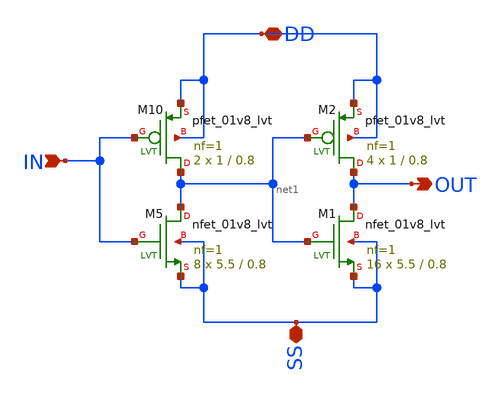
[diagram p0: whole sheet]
** sch_path: xschem/ring_100mV_buffer.sch
**.subckt ring_100mV_buffer OUT DD SS IN
*.opin OUT
*.iopin DD
*.iopin SS
*.ipin IN
XM5 net1 IN SS SS sky130_fd_pr__nfet_01v8_lvt L=0.8 W=5.5 nf=1 ad='int((nf+1)/2) * W/nf * 0.29' as='int((nf+2)/2) * W/nf * 0.29'
+ pd='2*int((nf+1)/2) * (W/nf + 0.29)' ps='2*int((nf+2)/2) * (W/nf + 0.29)' nrd='0.29 / W' nrs='0.29 / W'
+ sa=0 sb=0 sd=0 mult=8 m=8
XM10 net1 IN DD DD sky130_fd_pr__pfet_01v8_lvt L=0.8 W=1 nf=1 ad='int((nf+1)/2) * W/nf * 0.29' as='int((nf+2)/2) * W/nf * 0.29'
+ pd='2*int((nf+1)/2) * (W/nf + 0.29)' ps='2*int((nf+2)/2) * (W/nf + 0.29)' nrd='0.29 / W' nrs='0.29 / W'
+ sa=0 sb=0 sd=0 mult=2 m=2
XM1 OUT net1 SS SS sky130_fd_pr__nfet_01v8_lvt L=0.8 W=5.5 nf=1 ad='int((nf+1)/2) * W/nf * 0.29' as='int((nf+2)/2) * W/nf * 0.29'
+ pd='2*int((nf+1)/2) * (W/nf + 0.29)' ps='2*int((nf+2)/2) * (W/nf + 0.29)' nrd='0.29 / W' nrs='0.29 / W'
+ sa=0 sb=0 sd=0 mult=16 m=16
XM2 OUT net1 DD DD sky130_fd_pr__pfet_01v8_lvt L=0.8 W=1 nf=1 ad='int((nf+1)/2) * W/nf * 0.29' as='int((nf+2)/2) * W/nf * 0.29'
+ pd='2*int((nf+1)/2) * (W/nf + 0.29)' ps='2*int((nf+2)/2) * (W/nf + 0.29)' nrd='0.29 / W' nrs='0.29 / W'
+ sa=0 sb=0 sd=0 mult=4 m=4
**.ends
.end
